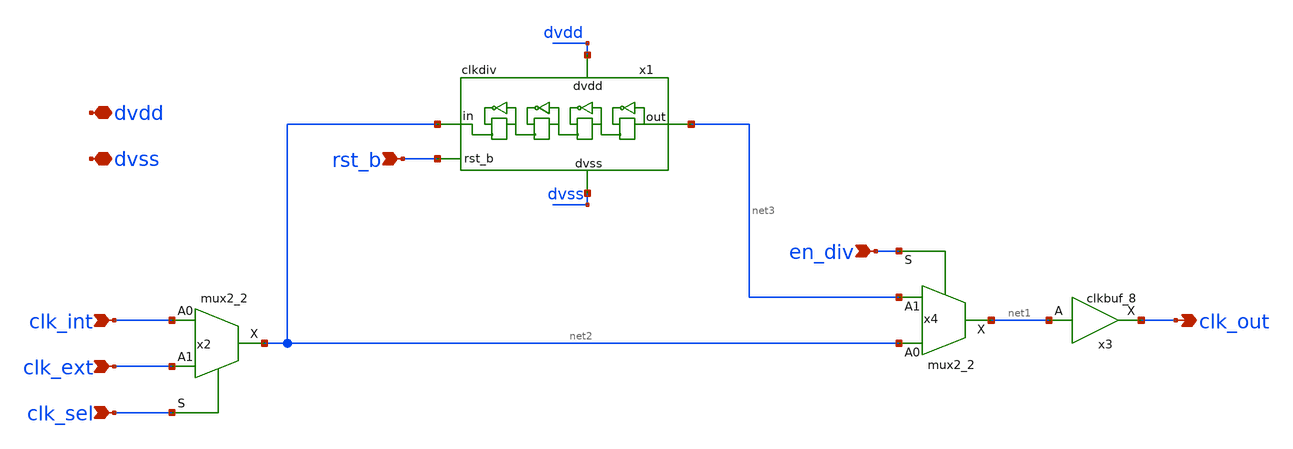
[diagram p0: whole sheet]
** sch_path: xschem/clksel/clksel.sch
**.subckt clksel clk_int rst_b clk_out dvdd dvss clk_ext en_div clk_sel
*.ipin clk_int
*.ipin rst_b
*.opin clk_out
*.iopin dvdd
*.iopin dvss
*.ipin clk_ext
*.ipin en_div
*.ipin clk_sel
x1 dvss net2 net3 rst_b dvdd clkdiv
x2 clk_int clk_ext clk_sel dvss dvss dvdd dvdd net2 sky130_fd_sc_hd__mux2_2
x3 net1 dvss dvss dvdd dvdd clk_out sky130_fd_sc_hd__clkbuf_8
x4 net2 net3 en_div dvss dvss dvdd dvdd net1 sky130_fd_sc_hd__mux2_2
**.ends

* expanding   symbol:  clkdiv/clkdiv.sym # of pins=5
** sym_path: xschem/clkdiv/clkdiv.sym
** sch_path: xschem/clkdiv/clkdiv.sch
.subckt clkdiv dvss in out rst_b dvdd
*.ipin in
*.ipin rst_b
*.opin out
*.iopin dvdd
*.iopin dvss
x6 in net1 rst_b dvss dvss dvdd dvdd div2 net5 sky130_fd_sc_hd__dfrbp_1
x8 div2 dvss dvss dvdd dvdd net1 sky130_fd_sc_hd__inv_1
* noconn #net5
x1 div2 net2 rst_b dvss dvss dvdd dvdd div4 net6 sky130_fd_sc_hd__dfrbp_1
x2 div4 dvss dvss dvdd dvdd net2 sky130_fd_sc_hd__inv_1
* noconn #net6
x3 div4 net3 rst_b dvss dvss dvdd dvdd div8 net7 sky130_fd_sc_hd__dfrbp_1
x4 div8 dvss dvss dvdd dvdd net3 sky130_fd_sc_hd__inv_1
* noconn #net7
x5 div8 net4 rst_b dvss dvss dvdd dvdd out net8 sky130_fd_sc_hd__dfrbp_1
x7 out dvss dvss dvdd dvdd net4 sky130_fd_sc_hd__inv_1
* noconn #net8
xdec[7] dvss dvss dvdd dvdd sky130_fd_sc_hd__decap_4
xdec[6] dvss dvss dvdd dvdd sky130_fd_sc_hd__decap_4
xdec[5] dvss dvss dvdd dvdd sky130_fd_sc_hd__decap_4
xdec[4] dvss dvss dvdd dvdd sky130_fd_sc_hd__decap_4
xdec[3] dvss dvss dvdd dvdd sky130_fd_sc_hd__decap_4
xdec[2] dvss dvss dvdd dvdd sky130_fd_sc_hd__decap_4
xdec[1] dvss dvss dvdd dvdd sky130_fd_sc_hd__decap_4
xdec[0] dvss dvss dvdd dvdd sky130_fd_sc_hd__decap_4
xtap dvss dvdd sky130_fd_sc_hd__tapvpwrvgnd_1
.ends

.end
